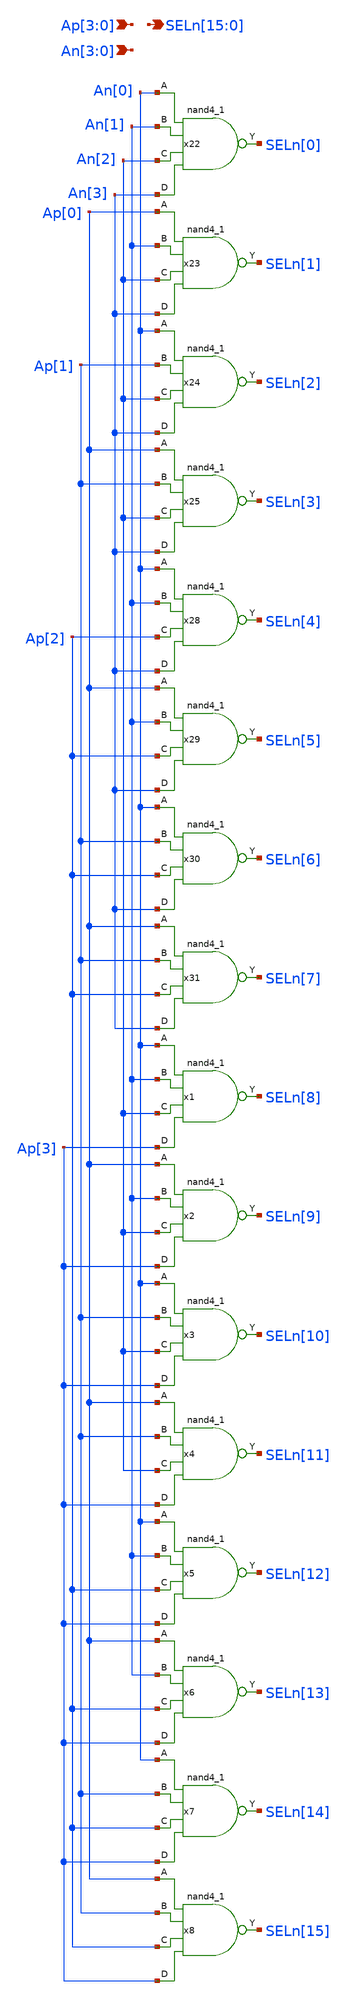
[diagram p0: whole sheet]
** sch_path: blocks/rom/rom_dec_4b.sch
**.subckt rom_dec_4b
*+ SELn[15],SELn[14],SELn[13],SELn[12],SELn[11],SELn[10],SELn[9],SELn[8],SELn[7],SELn[6],SELn[5],SELn[4],SELn[3],SELn[2],SELn[1],SELn[0] Ap[3],Ap[2],Ap[1],Ap[0] An[3],An[2],An[1],An[0]
*.opin
*+ SELn[15],SELn[14],SELn[13],SELn[12],SELn[11],SELn[10],SELn[9],SELn[8],SELn[7],SELn[6],SELn[5],SELn[4],SELn[3],SELn[2],SELn[1],SELn[0]
*.ipin Ap[3],Ap[2],Ap[1],Ap[0]
*.ipin An[3],An[2],An[1],An[0]
x22 An[0] An[1] An[2] An[3] VSS VSS VCC VCC SELn[0] sky130_fd_sc_hd__nand4_1
x23 Ap[0] An[1] An[2] An[3] VSS VSS VCC VCC SELn[1] sky130_fd_sc_hd__nand4_1
x24 An[0] Ap[1] An[2] An[3] VSS VSS VCC VCC SELn[2] sky130_fd_sc_hd__nand4_1
x25 Ap[0] Ap[1] An[2] An[3] VSS VSS VCC VCC SELn[3] sky130_fd_sc_hd__nand4_1
x28 An[0] An[1] Ap[2] An[3] VSS VSS VCC VCC SELn[4] sky130_fd_sc_hd__nand4_1
x29 Ap[0] An[1] Ap[2] An[3] VSS VSS VCC VCC SELn[5] sky130_fd_sc_hd__nand4_1
x30 An[0] Ap[1] Ap[2] An[3] VSS VSS VCC VCC SELn[6] sky130_fd_sc_hd__nand4_1
x31 Ap[0] Ap[1] Ap[2] An[3] VSS VSS VCC VCC SELn[7] sky130_fd_sc_hd__nand4_1
x1 An[0] An[1] An[2] Ap[3] VSS VSS VCC VCC SELn[8] sky130_fd_sc_hd__nand4_1
x2 Ap[0] An[1] An[2] Ap[3] VSS VSS VCC VCC SELn[9] sky130_fd_sc_hd__nand4_1
x3 An[0] Ap[1] An[2] Ap[3] VSS VSS VCC VCC SELn[10] sky130_fd_sc_hd__nand4_1
x4 Ap[0] Ap[1] An[2] Ap[3] VSS VSS VCC VCC SELn[11] sky130_fd_sc_hd__nand4_1
x5 An[0] An[1] Ap[2] Ap[3] VSS VSS VCC VCC SELn[12] sky130_fd_sc_hd__nand4_1
x6 Ap[0] An[1] Ap[2] Ap[3] VSS VSS VCC VCC SELn[13] sky130_fd_sc_hd__nand4_1
x7 An[0] Ap[1] Ap[2] Ap[3] VSS VSS VCC VCC SELn[14] sky130_fd_sc_hd__nand4_1
x8 Ap[0] Ap[1] Ap[2] Ap[3] VSS VSS VCC VCC SELn[15] sky130_fd_sc_hd__nand4_1
**.ends
.end
